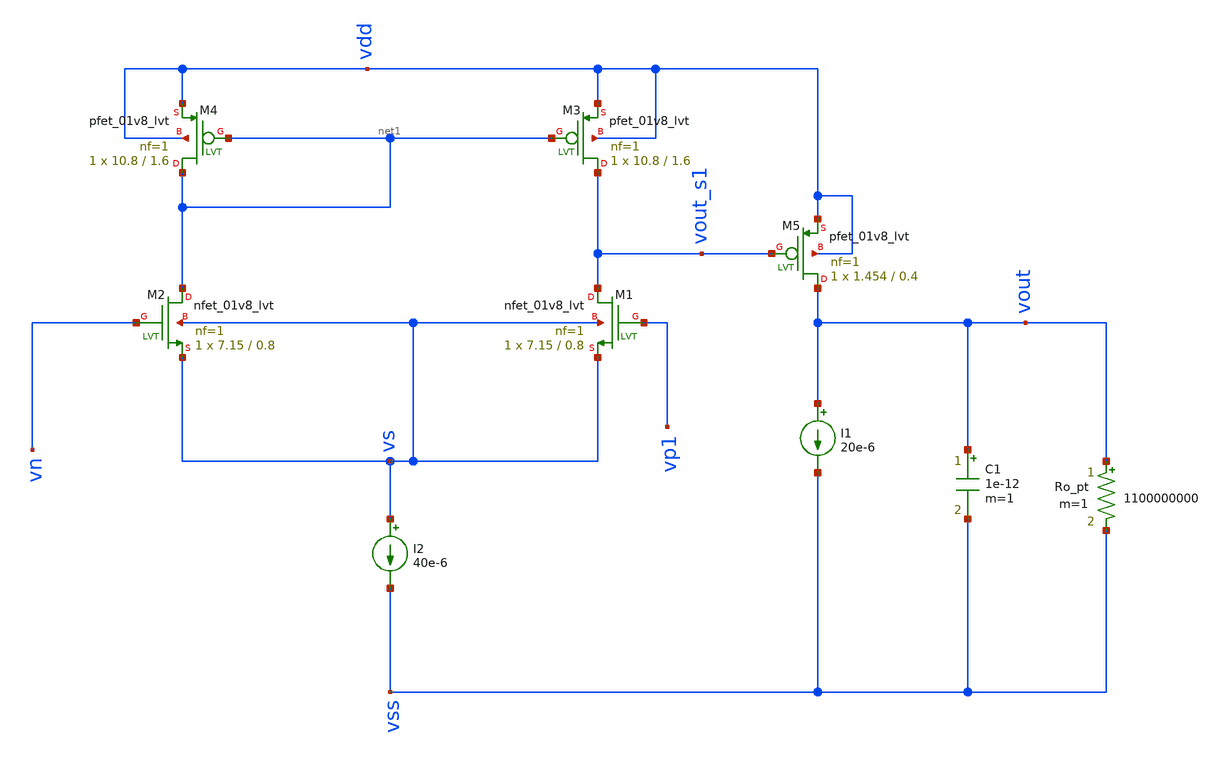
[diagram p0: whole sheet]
** sch_path: test/sstadex/xschem/stage2_OTA_tb_sim.sch
**.subckt stage2_OTA_tb_sim
I2 vs vss 40e-6
XM1 vout_s1 vp1 vs vs sky130_fd_pr__nfet_01v8_lvt L=0.8 W=7.15 nf=1 ad='int((nf+1)/2) * W/nf * 0.29'
+ as='int((nf+2)/2) * W/nf * 0.29' pd='2*int((nf+1)/2) * (W/nf + 0.29)' ps='2*int((nf+2)/2) * (W/nf + 0.29)'
+ nrd='0.29 / W' nrs='0.29 / W' sa=0 sb=0 sd=0 mult=1 m=1
XM2 net1 vn vs vs sky130_fd_pr__nfet_01v8_lvt L=0.8 W=7.15 nf=1 ad='int((nf+1)/2) * W/nf * 0.29' as='int((nf+2)/2) * W/nf * 0.29'
+ pd='2*int((nf+1)/2) * (W/nf + 0.29)' ps='2*int((nf+2)/2) * (W/nf + 0.29)' nrd='0.29 / W' nrs='0.29 / W'
+ sa=0 sb=0 sd=0 mult=1 m=1
XM3 vout_s1 net1 vdd vdd sky130_fd_pr__pfet_01v8_lvt L=1.6 W=10.8 nf=1 ad='int((nf+1)/2) * W/nf * 0.29'
+ as='int((nf+2)/2) * W/nf * 0.29' pd='2*int((nf+1)/2) * (W/nf + 0.29)' ps='2*int((nf+2)/2) * (W/nf + 0.29)'
+ nrd='0.29 / W' nrs='0.29 / W' sa=0 sb=0 sd=0 mult=1 m=1
XM4 net1 net1 vdd vdd sky130_fd_pr__pfet_01v8_lvt L=1.6 W=10.8 nf=1 ad='int((nf+1)/2) * W/nf * 0.29'
+ as='int((nf+2)/2) * W/nf * 0.29' pd='2*int((nf+1)/2) * (W/nf + 0.29)' ps='2*int((nf+2)/2) * (W/nf + 0.29)'
+ nrd='0.29 / W' nrs='0.29 / W' sa=0 sb=0 sd=0 mult=1 m=1
XM5 vout vout_s1 vdd vdd sky130_fd_pr__pfet_01v8_lvt L=0.4 W=1.454 nf=1 ad='int((nf+1)/2) * W/nf * 0.29'
+ as='int((nf+2)/2) * W/nf * 0.29' pd='2*int((nf+1)/2) * (W/nf + 0.29)' ps='2*int((nf+2)/2) * (W/nf + 0.29)'
+ nrd='0.29 / W' nrs='0.29 / W' sa=0 sb=0 sd=0 mult=1 m=1
I1 vout vss 20e-6
C1 vout vss 1e-12 m=1
Ro_pt vout vss 1100000000 m=1
**** begin user architecture code



.lib /opt/pdks/sky130A/libs.tech/ngspice/sky130.lib.spice tt

Vref vn 0 0.9
Vdd vdd 0 1.8
Vpos vp1 0 0.9 ac 1
Vss vss 0 0

.control
ac dec 10 1 1G
plot vdb(vout)
plot phase(vout)
op
print vout vs vout_s1
.endc



**** end user architecture code
**.ends
.end
